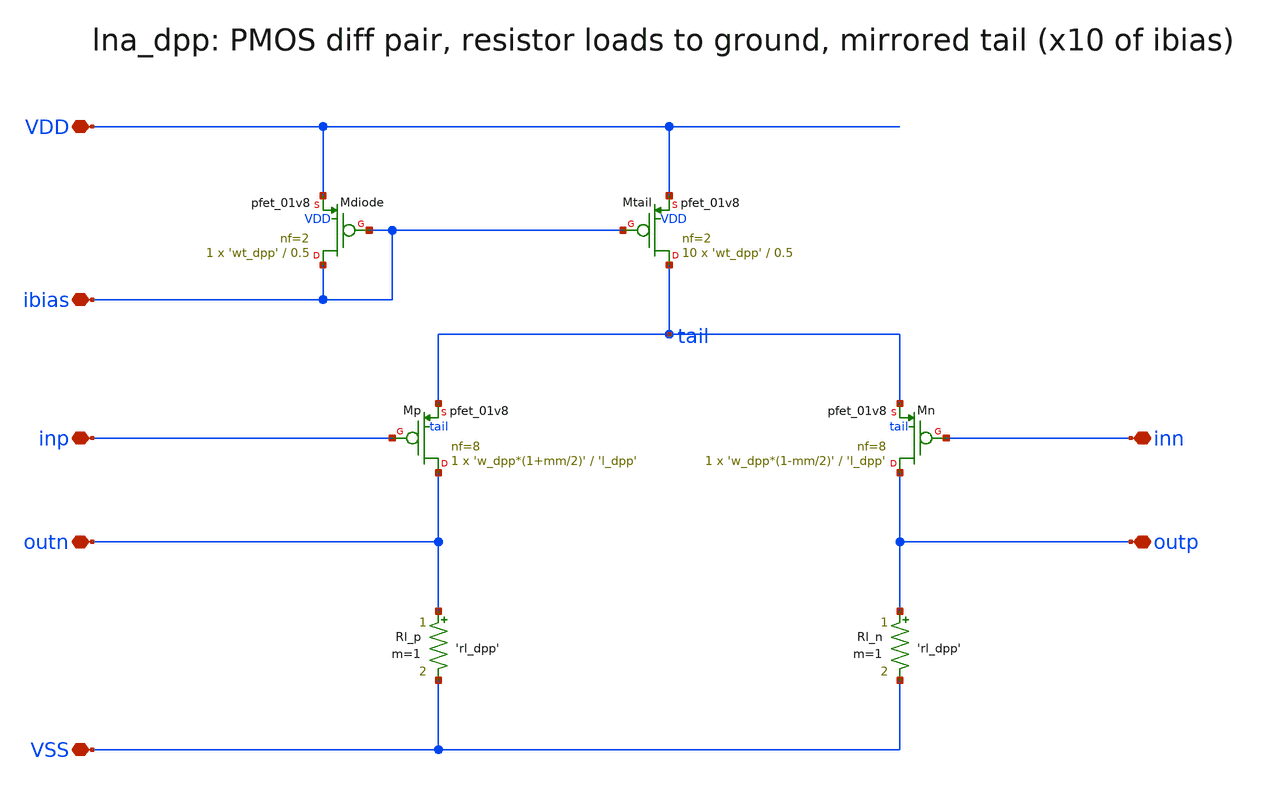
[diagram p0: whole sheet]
** sch_path: xschem/lna_dpp.sch
**.subckt lna_dpp VDD VSS ibias inp inn outp outn
*.iopin VDD
*.iopin VSS
*.iopin ibias
*.iopin inp
*.iopin inn
*.iopin outp
*.iopin outn
XMtail tail ibias VDD VDD sky130_fd_pr__pfet_01v8 L=0.5 W='wt_dpp' nf=2 ad='int((nf+1)/2) * W/nf * 0.29'
+ as='int((nf+2)/2) * W/nf * 0.29' pd='2*int((nf+1)/2) * (W/nf + 0.29)' ps='2*int((nf+2)/2) * (W/nf + 0.29)'
+ nrd='0.29 / W' nrs='0.29 / W' sa=0 sb=0 sd=0 mult=10 m=10
XMdiode ibias ibias VDD VDD sky130_fd_pr__pfet_01v8 L=0.5 W='wt_dpp' nf=2 ad='int((nf+1)/2) * W/nf * 0.29'
+ as='int((nf+2)/2) * W/nf * 0.29' pd='2*int((nf+1)/2) * (W/nf + 0.29)' ps='2*int((nf+2)/2) * (W/nf + 0.29)'
+ nrd='0.29 / W' nrs='0.29 / W' sa=0 sb=0 sd=0 mult=1 m=1
XMp outn inp tail tail sky130_fd_pr__pfet_01v8 L='l_dpp' W='w_dpp*(1+mm/2)' nf=8 ad='int((nf+1)/2) * W/nf * 0.29'
+ as='int((nf+2)/2) * W/nf * 0.29' pd='2*int((nf+1)/2) * (W/nf + 0.29)' ps='2*int((nf+2)/2) * (W/nf + 0.29)'
+ nrd='0.29 / W' nrs='0.29 / W' sa=0 sb=0 sd=0 mult=1 m=1
Rl_p outn VSS 'rl_dpp' m=1
XMn outp inn tail tail sky130_fd_pr__pfet_01v8 L='l_dpp' W='w_dpp*(1-mm/2)' nf=8 ad='int((nf+1)/2) * W/nf * 0.29'
+ as='int((nf+2)/2) * W/nf * 0.29' pd='2*int((nf+1)/2) * (W/nf + 0.29)' ps='2*int((nf+2)/2) * (W/nf + 0.29)'
+ nrd='0.29 / W' nrs='0.29 / W' sa=0 sb=0 sd=0 mult=1 m=1
Rl_n outp VSS 'rl_dpp' m=1
**.ends
.end
